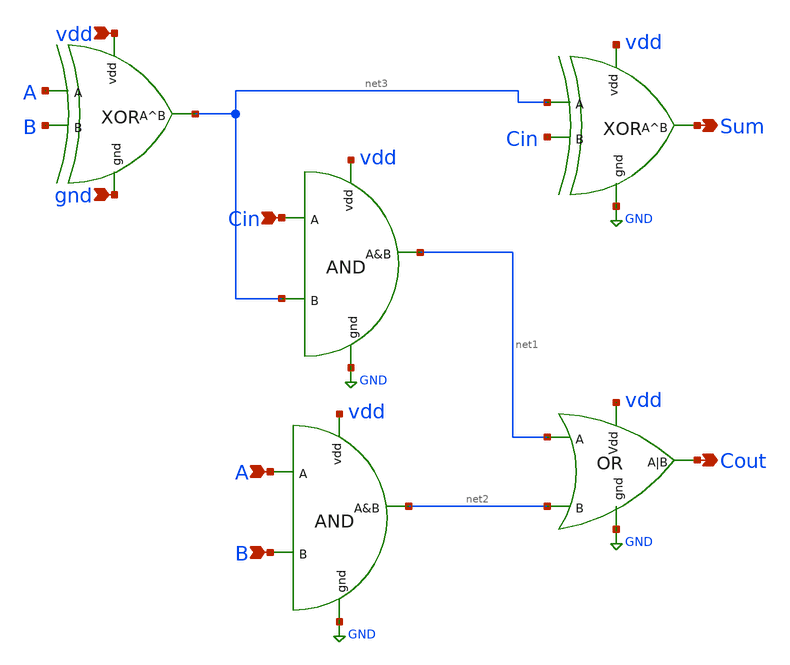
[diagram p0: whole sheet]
** sch_path: schematics/full_adder.sch
**.subckt full_adder vdd gnd A B Cin Sum Cout
*.ipin vdd
*.ipin gnd
*.ipin A
*.ipin B
*.ipin Cin
*.opin Sum
*.opin Cout
x1 vdd gnd net3 A B xor
x2 vdd GND Sum net3 Cin xor
x3 Cin net3 net1 vdd GND and
x4 A B net2 vdd GND and
x5 vdd GND Cout net1 net2 or
**.ends
.GLOBAL GND
.end
